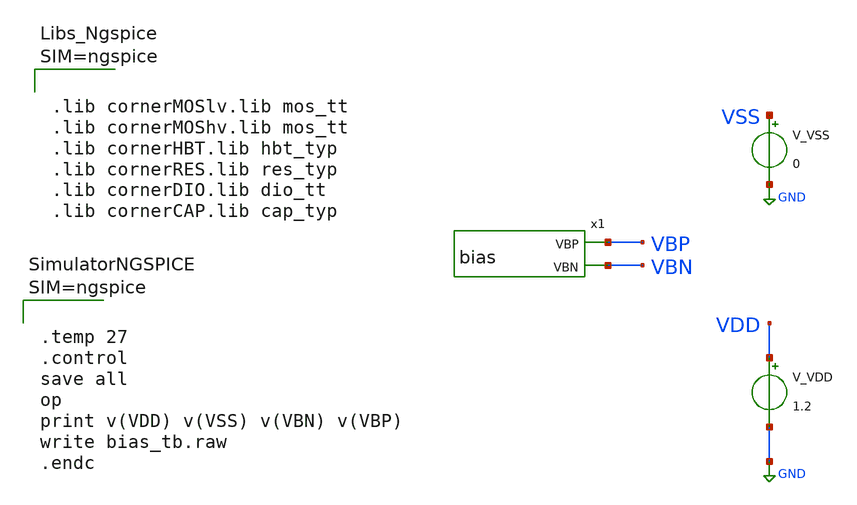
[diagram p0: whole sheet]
** sch_path: design/blocks/bias/schematic/bias_tb.sch
**.subckt bias_tb
x1 VBP VBN VDD VSS bias
V_VDD VDD GND 1.2
V_VSS VSS GND 0
**** begin user architecture code



.lib cornerMOSlv.lib mos_tt
.lib cornerMOShv.lib mos_tt
.lib cornerHBT.lib hbt_typ
.lib cornerRES.lib res_typ
.lib cornerDIO.lib dio_tt
.lib cornerCAP.lib cap_typ






.temp 27
.control
save all
op
print v(VDD) v(VSS) v(VBN) v(VBP)
write bias_tb.raw
.endc



**** end user architecture code
**.ends

* expanding   symbol:  bias.sym # of pins=2
** sym_path: design/blocks/bias/schematic/bias.sym
** sch_path: design/blocks/bias/schematic/bias.sch
.subckt bias VBP VBN VDD VSS
*.opin VBP
*.opin VBN
XM1 VBN VBN VSS VSS sg13_lv_nmos w=2u l=1u ng=1 m=1 mm_ok=1
XM2 VBP VBP VDD VDD sg13_lv_pmos w=2u l=1u ng=1 m=1 mm_ok=1
XR2 VBP VSS sub! rhigh w=0.5e-6 l=10.0e-6 m=1 b=0 mm_ok=1
XR1 VDD VBN sub! rhigh w=0.5e-6 l=10.0e-6 m=1 b=0 mm_ok=1
XC1 VBN VSS cap_cmim w=26.0e-6 l=26.0e-6 m=1 mm_ok=1
XC2 VDD VBP cap_cmim w=26.0e-6 l=26.0e-6 m=1 mm_ok=1
.ends

.GLOBAL GND
.end
